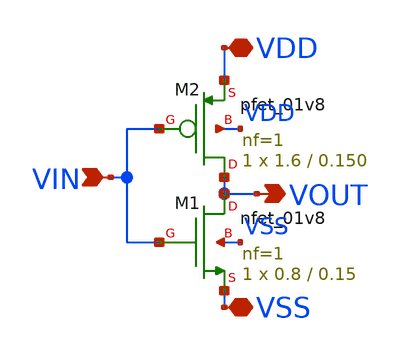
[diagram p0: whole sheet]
** sch_path: xschem/xschem_BGR_Top/Sigma_Delta/Inverter_02/Inverter_02.sch
**.subckt Inverter_02 VIN VDD VSS VOUT
*.ipin VIN
*.iopin VDD
*.iopin VSS
*.opin VOUT
XM1 VOUT VIN VSS VSS sky130_fd_pr__nfet_01v8 L=0.15 W=0.8 nf=1 ad='int((nf+1)/2) * W/nf * 0.29' as='int((nf+2)/2) * W/nf * 0.29'
+ pd='2*int((nf+1)/2) * (W/nf + 0.29)' ps='2*int((nf+2)/2) * (W/nf + 0.29)' nrd='0.29 / W' nrs='0.29 / W'
+ sa=0 sb=0 sd=0 mult=1 m=1
XM2 VOUT VIN VDD VDD sky130_fd_pr__pfet_01v8 L=0.150 W=1.6 nf=1 ad='int((nf+1)/2) * W/nf * 0.29' as='int((nf+2)/2) * W/nf * 0.29'
+ pd='2*int((nf+1)/2) * (W/nf + 0.29)' ps='2*int((nf+2)/2) * (W/nf + 0.29)' nrd='0.29 / W' nrs='0.29 / W'
+ sa=0 sb=0 sd=0 mult=1 m=1
**** begin user architecture code

** opencircuitdesign pdks install
.lib $::SKYWATER_MODELS/sky130.lib.spice tt


**** end user architecture code
**.ends
.end
